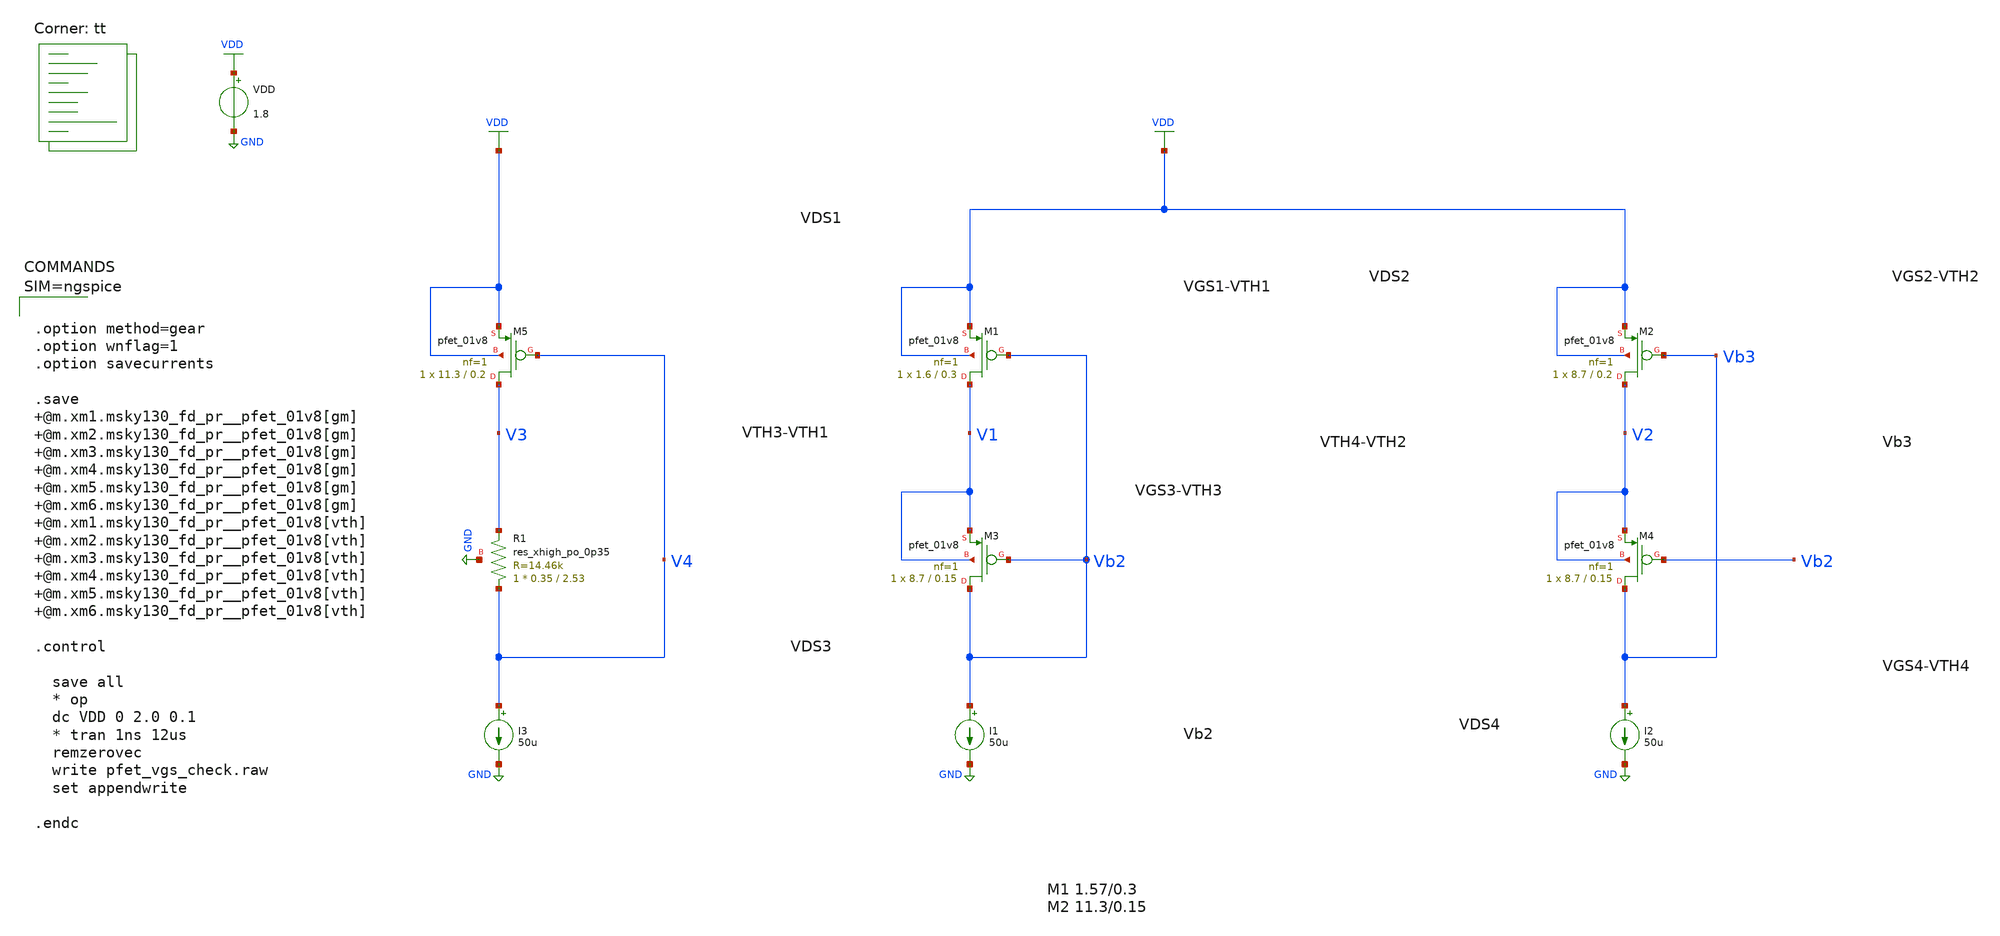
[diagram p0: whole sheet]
** sch_path: projects/opamp/xschem_ngspice/pfet_vgs_check.sch
**.subckt pfet_vgs_check
XM3 Vb2 Vb2 V1 V1 sky130_fd_pr__pfet_01v8 L=0.15 W=8.7 nf=1 ad='int((nf+1)/2) * W/nf * 0.29' as='int((nf+2)/2) * W/nf * 0.29'
+ pd='2*int((nf+1)/2) * (W/nf + 0.29)' ps='2*int((nf+2)/2) * (W/nf + 0.29)' nrd='0.29 / W' nrs='0.29 / W'
+ sa=0 sb=0 sd=0 mult=1 m=1
XM4 Vb3 Vb2 V2 V2 sky130_fd_pr__pfet_01v8 L=0.15 W=8.7 nf=1 ad='int((nf+1)/2) * W/nf * 0.29' as='int((nf+2)/2) * W/nf * 0.29'
+ pd='2*int((nf+1)/2) * (W/nf + 0.29)' ps='2*int((nf+2)/2) * (W/nf + 0.29)' nrd='0.29 / W' nrs='0.29 / W'
+ sa=0 sb=0 sd=0 mult=1 m=1
XM1 V1 Vb2 VDD VDD sky130_fd_pr__pfet_01v8 L=0.3 W=1.6 nf=1 ad='int((nf+1)/2) * W/nf * 0.29' as='int((nf+2)/2) * W/nf * 0.29'
+ pd='2*int((nf+1)/2) * (W/nf + 0.29)' ps='2*int((nf+2)/2) * (W/nf + 0.29)' nrd='0.29 / W' nrs='0.29 / W'
+ sa=0 sb=0 sd=0 mult=1 m=1
XM2 V2 Vb3 VDD VDD sky130_fd_pr__pfet_01v8 L=0.2 W=8.7 nf=1 ad='int((nf+1)/2) * W/nf * 0.29' as='int((nf+2)/2) * W/nf * 0.29'
+ pd='2*int((nf+1)/2) * (W/nf + 0.29)' ps='2*int((nf+2)/2) * (W/nf + 0.29)' nrd='0.29 / W' nrs='0.29 / W'
+ sa=0 sb=0 sd=0 mult=1 m=1
I1 Vb2 GND 50u
I2 Vb3 GND 50u
VDD VDD GND 1.8
XM5 V3 V4 VDD VDD sky130_fd_pr__pfet_01v8 L=0.2 W=11.3 nf=1 ad='int((nf+1)/2) * W/nf * 0.29' as='int((nf+2)/2) * W/nf * 0.29'
+ pd='2*int((nf+1)/2) * (W/nf + 0.29)' ps='2*int((nf+2)/2) * (W/nf + 0.29)' nrd='0.29 / W' nrs='0.29 / W'
+ sa=0 sb=0 sd=0 mult=1 m=1
I3 V4 GND 50u
XR1 V4 V3 GND sky130_fd_pr__res_xhigh_po_0p35 L=2.53 mult=1 m=1
**** begin user architecture code



.option method=gear
.option wnflag=1
.option savecurrents

.save @m.xm1.msky130_fd_pr__pfet_01v8[gm] @m.xm2.msky130_fd_pr__pfet_01v8[gm] @m.xm3.msky130_fd_pr__pfet_01v8[gm] @m.xm4.msky130_fd_pr__pfet_01v8[gm] @m.xm5.msky130_fd_pr__pfet_01v8[gm] @m.xm6.msky130_fd_pr__pfet_01v8[gm] @m.xm1.msky130_fd_pr__pfet_01v8[vth] @m.xm2.msky130_fd_pr__pfet_01v8[vth] @m.xm3.msky130_fd_pr__pfet_01v8[vth] @m.xm4.msky130_fd_pr__pfet_01v8[vth] @m.xm5.msky130_fd_pr__pfet_01v8[vth] @m.xm6.msky130_fd_pr__pfet_01v8[vth]

.control

  save all
  * op
  dc VDD 0 2.0 0.1
  * tran 1ns 12us
  remzerovec
  write pfet_vgs_check.raw
  set appendwrite

.endc




.lib $::SKYWATER_MODELS/sky130.lib.spice tt
**** end user architecture code
**.ends
.GLOBAL VDD
.GLOBAL GND
.end
